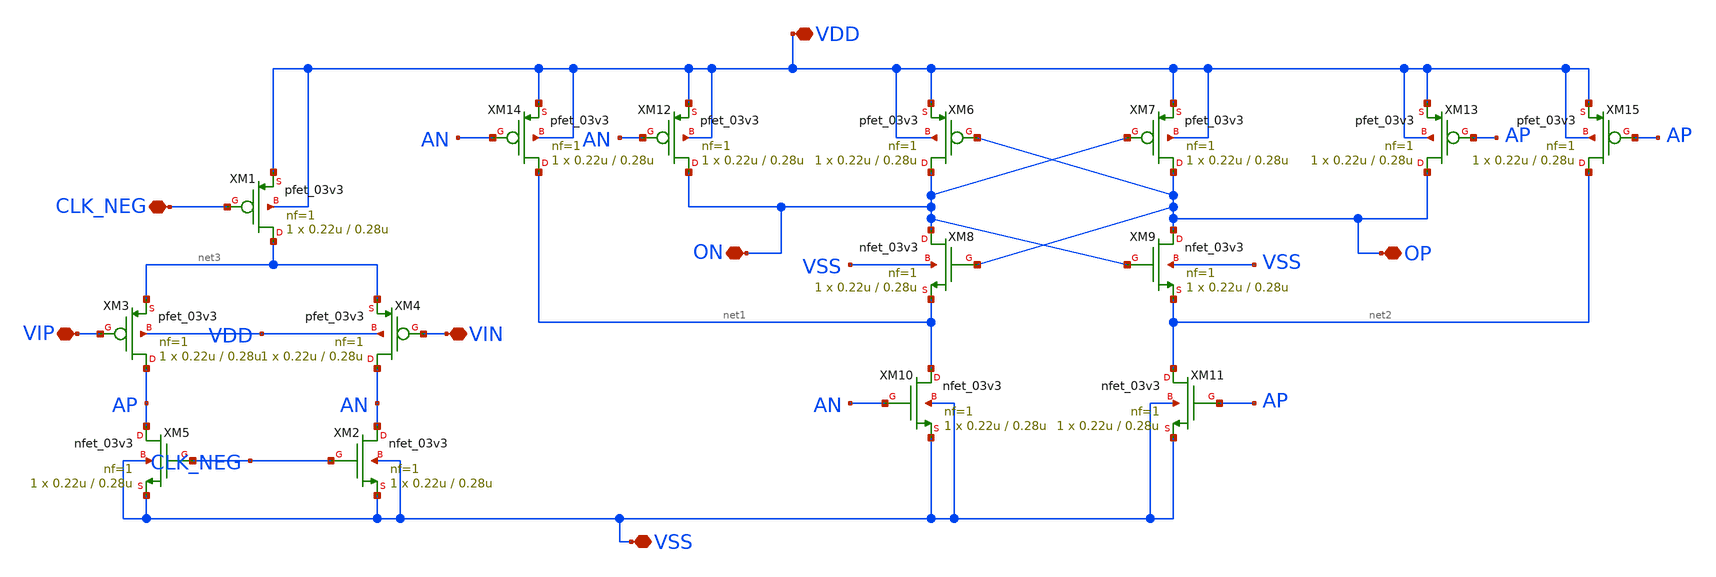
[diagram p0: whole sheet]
** sch_path: designs/sar_adc/comparator/comparador/xschem/comparador.sch
**.subckt comparador VSS VDD VIN VIP OP ON CLK_NEG
*.iopin VSS
*.iopin VDD
*.iopin VIN
*.iopin VIP
*.iopin OP
*.iopin ON
*.iopin CLK_NEG
XM1 net3 CLK_NEG VDD VDD pfet_03v3 L=0.28u W=0.22u nf=1 ad='int((nf+1)/2) * W/nf * 0.18u' as='int((nf+2)/2) * W/nf * 0.18u'
+ pd='2*int((nf+1)/2) * (W/nf + 0.18u)' ps='2*int((nf+2)/2) * (W/nf + 0.18u)' nrd='0.18u / W' nrs='0.18u / W'
+ sa=0 sb=0 sd=0 m=1
XM2 AN CLK_NEG VSS VSS nfet_03v3 L=0.28u W=0.22u nf=1 ad='int((nf+1)/2) * W/nf * 0.18u' as='int((nf+2)/2) * W/nf * 0.18u'
+ pd='2*int((nf+1)/2) * (W/nf + 0.18u)' ps='2*int((nf+2)/2) * (W/nf + 0.18u)' nrd='0.18u / W' nrs='0.18u / W'
+ sa=0 sb=0 sd=0 m=1
XM3 AP VIP net3 VDD pfet_03v3 L=0.28u W=0.22u nf=1 ad='int((nf+1)/2) * W/nf * 0.18u' as='int((nf+2)/2) * W/nf * 0.18u'
+ pd='2*int((nf+1)/2) * (W/nf + 0.18u)' ps='2*int((nf+2)/2) * (W/nf + 0.18u)' nrd='0.18u / W' nrs='0.18u / W'
+ sa=0 sb=0 sd=0 m=1
XM4 AN VIN net3 VDD pfet_03v3 L=0.28u W=0.22u nf=1 ad='int((nf+1)/2) * W/nf * 0.18u' as='int((nf+2)/2) * W/nf * 0.18u'
+ pd='2*int((nf+1)/2) * (W/nf + 0.18u)' ps='2*int((nf+2)/2) * (W/nf + 0.18u)' nrd='0.18u / W' nrs='0.18u / W'
+ sa=0 sb=0 sd=0 m=1
XM5 AP CLK_NEG VSS VSS nfet_03v3 L=0.28u W=0.22u nf=1 ad='int((nf+1)/2) * W/nf * 0.18u' as='int((nf+2)/2) * W/nf * 0.18u'
+ pd='2*int((nf+1)/2) * (W/nf + 0.18u)' ps='2*int((nf+2)/2) * (W/nf + 0.18u)' nrd='0.18u / W' nrs='0.18u / W'
+ sa=0 sb=0 sd=0 m=1
XM6 ON OP VDD VDD pfet_03v3 L=0.28u W=0.22u nf=1 ad='int((nf+1)/2) * W/nf * 0.18u' as='int((nf+2)/2) * W/nf * 0.18u'
+ pd='2*int((nf+1)/2) * (W/nf + 0.18u)' ps='2*int((nf+2)/2) * (W/nf + 0.18u)' nrd='0.18u / W' nrs='0.18u / W'
+ sa=0 sb=0 sd=0 m=1
XM7 OP ON VDD VDD pfet_03v3 L=0.28u W=0.22u nf=1 ad='int((nf+1)/2) * W/nf * 0.18u' as='int((nf+2)/2) * W/nf * 0.18u'
+ pd='2*int((nf+1)/2) * (W/nf + 0.18u)' ps='2*int((nf+2)/2) * (W/nf + 0.18u)' nrd='0.18u / W' nrs='0.18u / W'
+ sa=0 sb=0 sd=0 m=1
XM8 ON OP net1 VSS nfet_03v3 L=0.28u W=0.22u nf=1 ad='int((nf+1)/2) * W/nf * 0.18u' as='int((nf+2)/2) * W/nf * 0.18u'
+ pd='2*int((nf+1)/2) * (W/nf + 0.18u)' ps='2*int((nf+2)/2) * (W/nf + 0.18u)' nrd='0.18u / W' nrs='0.18u / W'
+ sa=0 sb=0 sd=0 m=1
XM9 OP ON net2 VSS nfet_03v3 L=0.28u W=0.22u nf=1 ad='int((nf+1)/2) * W/nf * 0.18u' as='int((nf+2)/2) * W/nf * 0.18u'
+ pd='2*int((nf+1)/2) * (W/nf + 0.18u)' ps='2*int((nf+2)/2) * (W/nf + 0.18u)' nrd='0.18u / W' nrs='0.18u / W'
+ sa=0 sb=0 sd=0 m=1
XM10 net1 AN VSS VSS nfet_03v3 L=0.28u W=0.22u nf=1 ad='int((nf+1)/2) * W/nf * 0.18u' as='int((nf+2)/2) * W/nf * 0.18u'
+ pd='2*int((nf+1)/2) * (W/nf + 0.18u)' ps='2*int((nf+2)/2) * (W/nf + 0.18u)' nrd='0.18u / W' nrs='0.18u / W'
+ sa=0 sb=0 sd=0 m=1
XM11 net2 AP VSS VSS nfet_03v3 L=0.28u W=0.22u nf=1 ad='int((nf+1)/2) * W/nf * 0.18u' as='int((nf+2)/2) * W/nf * 0.18u'
+ pd='2*int((nf+1)/2) * (W/nf + 0.18u)' ps='2*int((nf+2)/2) * (W/nf + 0.18u)' nrd='0.18u / W' nrs='0.18u / W'
+ sa=0 sb=0 sd=0 m=1
XM12 ON AN VDD VDD pfet_03v3 L=0.28u W=0.22u nf=1 ad='int((nf+1)/2) * W/nf * 0.18u' as='int((nf+2)/2) * W/nf * 0.18u'
+ pd='2*int((nf+1)/2) * (W/nf + 0.18u)' ps='2*int((nf+2)/2) * (W/nf + 0.18u)' nrd='0.18u / W' nrs='0.18u / W'
+ sa=0 sb=0 sd=0 m=1
XM13 OP AP VDD VDD pfet_03v3 L=0.28u W=0.22u nf=1 ad='int((nf+1)/2) * W/nf * 0.18u' as='int((nf+2)/2) * W/nf * 0.18u'
+ pd='2*int((nf+1)/2) * (W/nf + 0.18u)' ps='2*int((nf+2)/2) * (W/nf + 0.18u)' nrd='0.18u / W' nrs='0.18u / W'
+ sa=0 sb=0 sd=0 m=1
XM14 net1 AN VDD VDD pfet_03v3 L=0.28u W=0.22u nf=1 ad='int((nf+1)/2) * W/nf * 0.18u' as='int((nf+2)/2) * W/nf * 0.18u'
+ pd='2*int((nf+1)/2) * (W/nf + 0.18u)' ps='2*int((nf+2)/2) * (W/nf + 0.18u)' nrd='0.18u / W' nrs='0.18u / W'
+ sa=0 sb=0 sd=0 m=1
XM15 net2 AP VDD VDD pfet_03v3 L=0.28u W=0.22u nf=1 ad='int((nf+1)/2) * W/nf * 0.18u' as='int((nf+2)/2) * W/nf * 0.18u'
+ pd='2*int((nf+1)/2) * (W/nf + 0.18u)' ps='2*int((nf+2)/2) * (W/nf + 0.18u)' nrd='0.18u / W' nrs='0.18u / W'
+ sa=0 sb=0 sd=0 m=1
**.ends
.end
